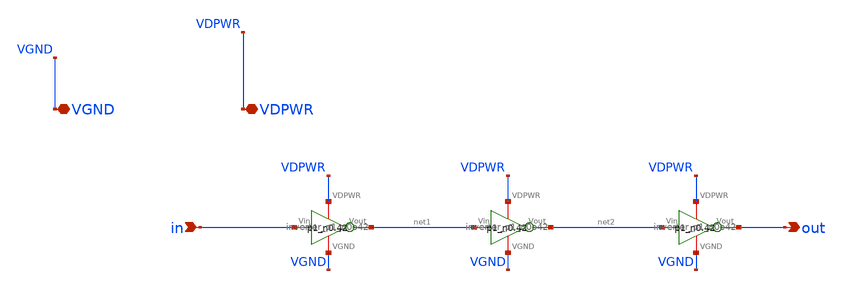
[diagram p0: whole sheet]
** sch_path: tt_um_emmersonv_tiq_adc/xschem/gain_stage.sch
**.subckt gain_stage in out VGND VDPWR
*.ipin in
*.opin out
*.iopin VGND
*.iopin VDPWR
x8 VDPWR net1 in VGND inverter_p1_n0o42
x9 VDPWR net2 net1 VGND inverter_p1_n0o42
x10 VDPWR out net2 VGND inverter_p1_n0o42
**.ends

* expanding   symbol:
*+  /foss/designs/analog-circuit-design/sky25a-TIQ_ADC/xschem/INVERTER_SIZES/inverter_p1_n0o42.sym # of pins=4
** sym_path: tt_um_emmersonv_tiq_adc/xschem/INVERTER_SIZES/inverter_p1_n0o42.sym
** sch_path: tt_um_emmersonv_tiq_adc/xschem/INVERTER_SIZES/inverter_p1_n0o42.sch
.subckt inverter_p1_n0o42 VDPWR Vout Vin VGND
*.opin Vout
*.ipin Vin
*.iopin VDPWR
*.iopin VGND
XM1 Vout Vin VGND VGND sky130_fd_pr__nfet_01v8 L=0.15 W=0.42 nf=1 ad='int((nf+1)/2) * W/nf * 0.29' as='int((nf+2)/2) * W/nf * 0.29'
+ pd='2*int((nf+1)/2) * (W/nf + 0.29)' ps='2*int((nf+2)/2) * (W/nf + 0.29)' nrd='0.29 / W' nrs='0.29 / W'
+ sa=0 sb=0 sd=0 mult=1 m=1
XM2 Vout Vin VDPWR VDPWR sky130_fd_pr__pfet_01v8 L=0.15 W=1 nf=1 ad='int((nf+1)/2) * W/nf * 0.29' as='int((nf+2)/2) * W/nf * 0.29'
+ pd='2*int((nf+1)/2) * (W/nf + 0.29)' ps='2*int((nf+2)/2) * (W/nf + 0.29)' nrd='0.29 / W' nrs='0.29 / W'
+ sa=0 sb=0 sd=0 mult=1 m=1
.ends

.end
